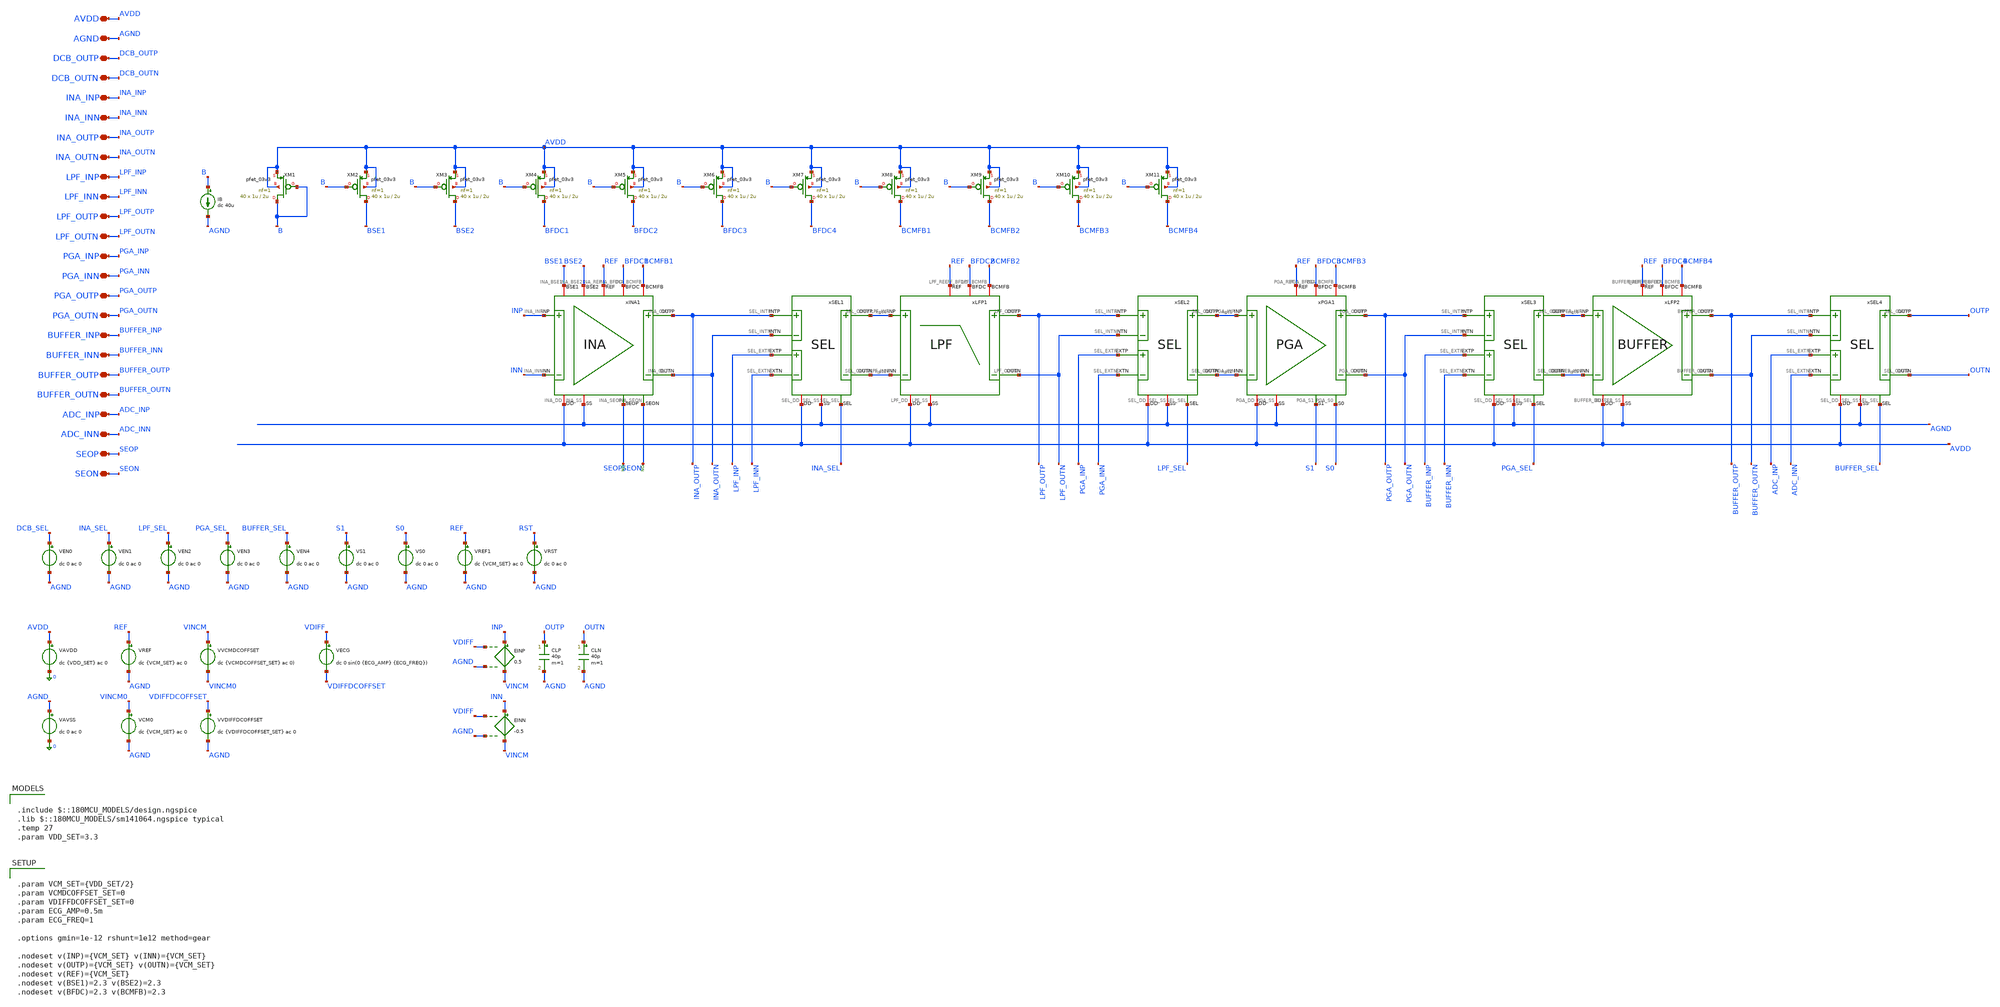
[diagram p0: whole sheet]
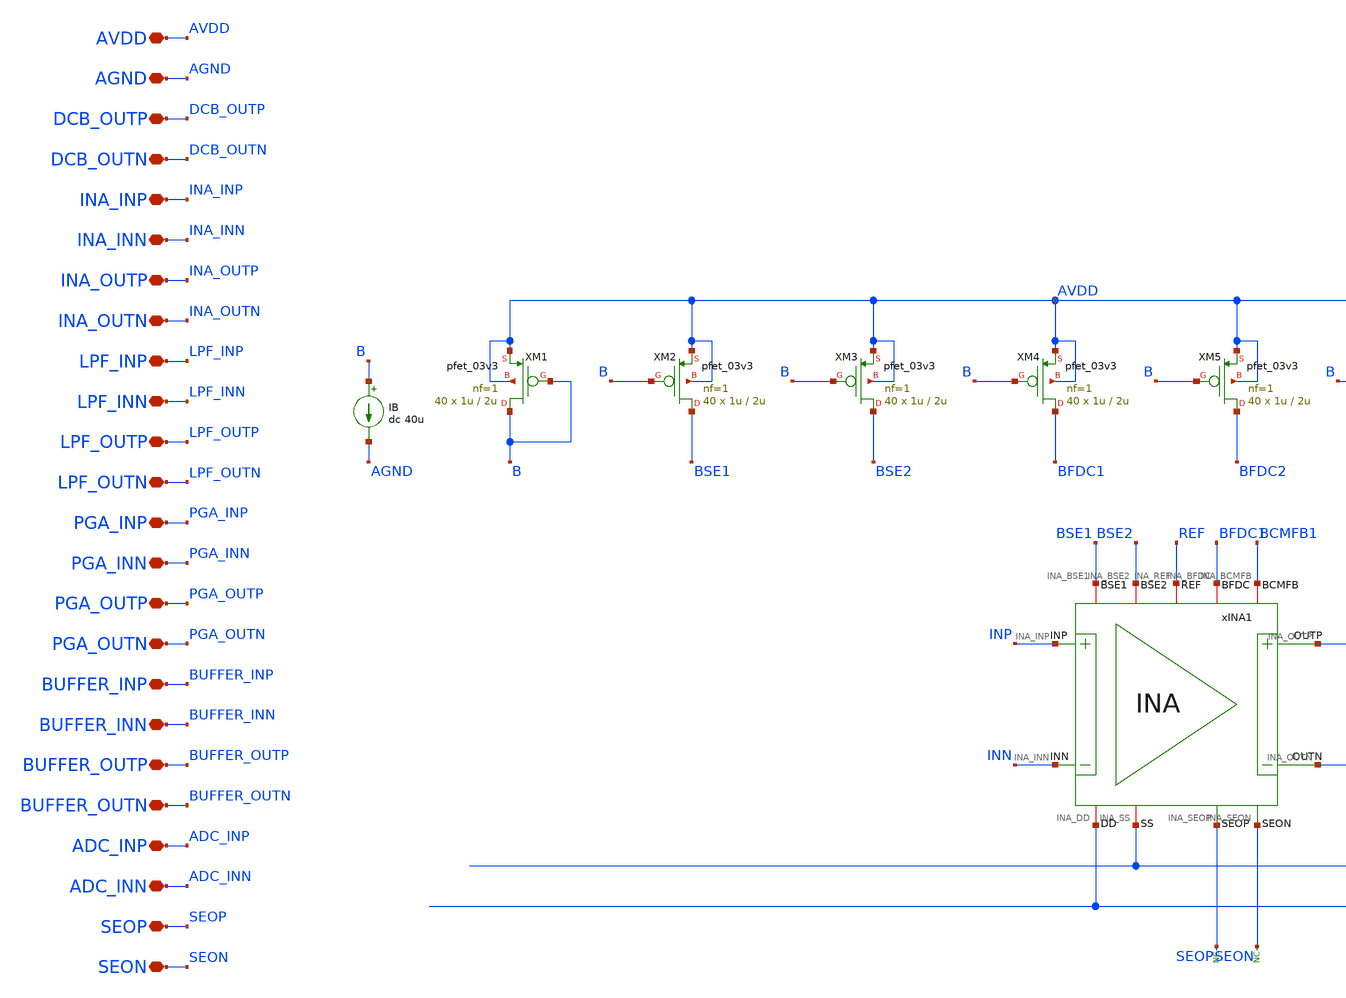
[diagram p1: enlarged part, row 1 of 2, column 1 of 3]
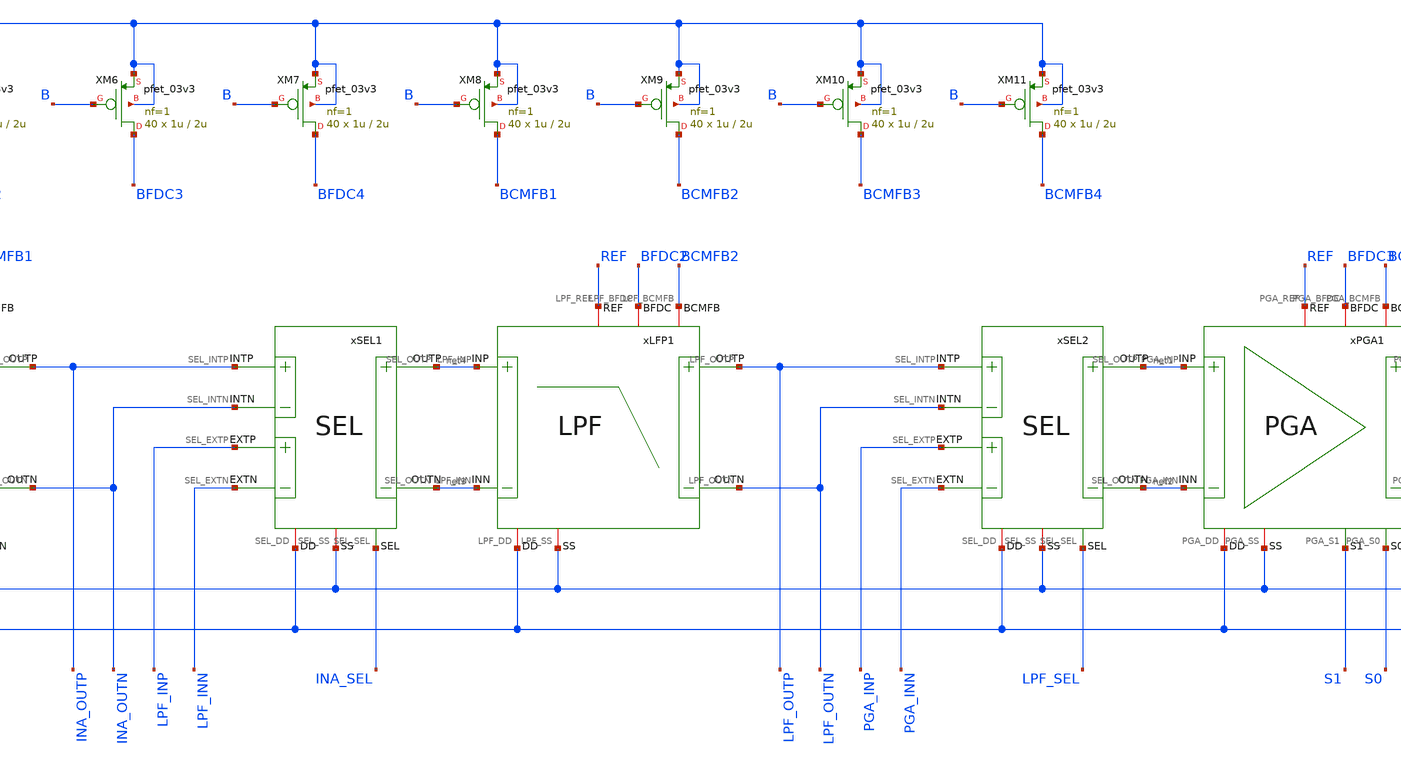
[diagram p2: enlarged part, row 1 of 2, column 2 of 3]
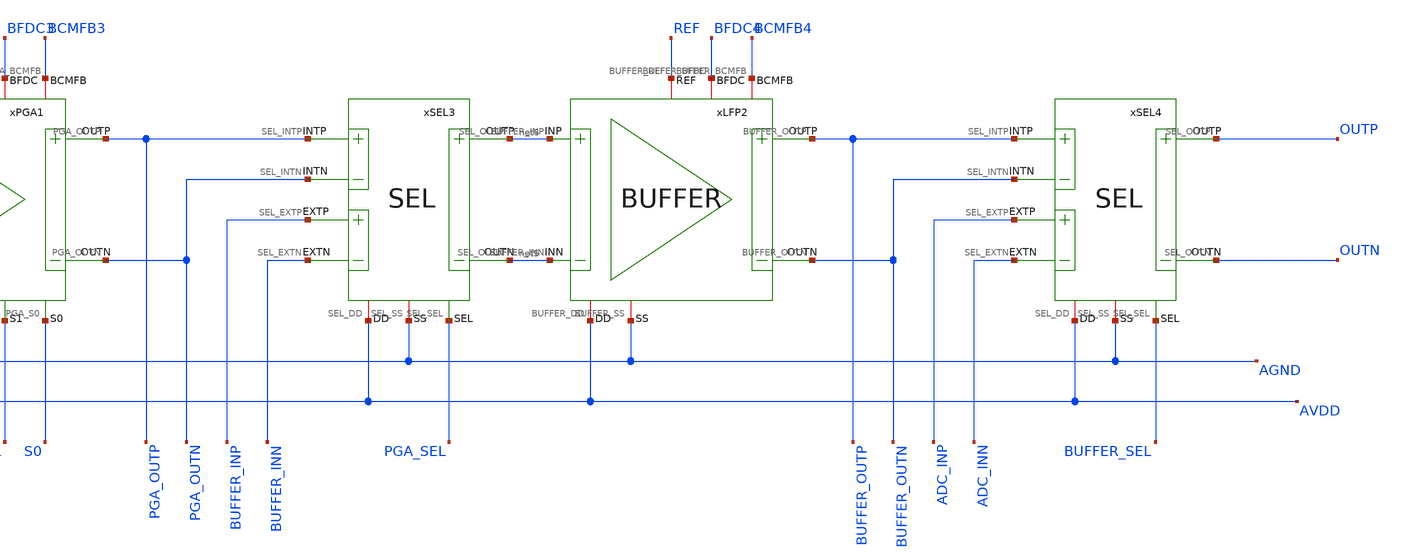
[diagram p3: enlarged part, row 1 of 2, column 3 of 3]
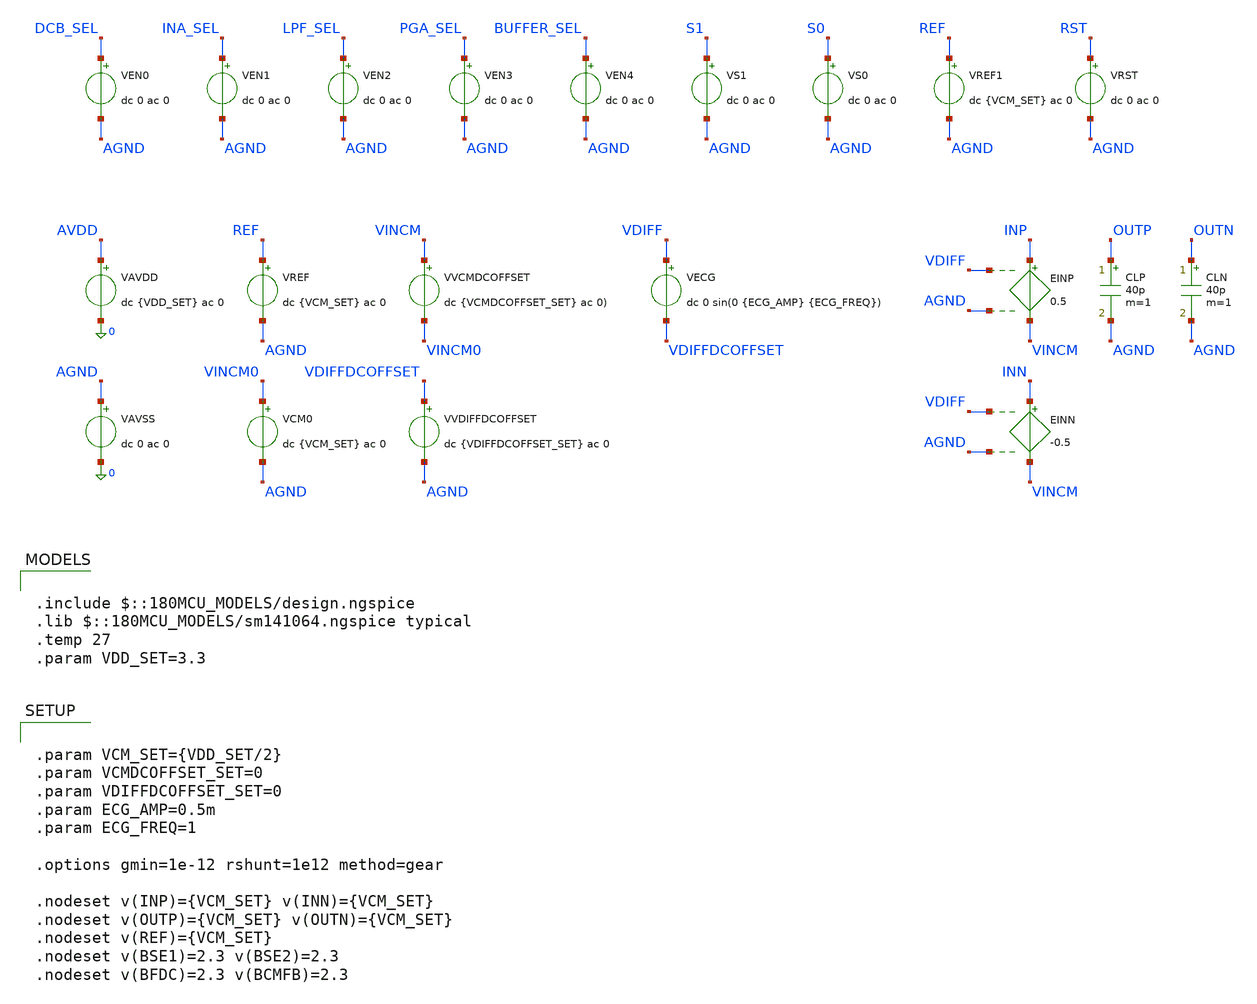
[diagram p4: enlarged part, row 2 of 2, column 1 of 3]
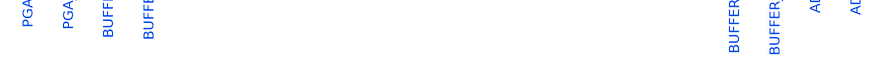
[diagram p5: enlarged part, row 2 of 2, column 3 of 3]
** sch_path: Design_Files/IC Design/Testbench/AFE/TRAN/AFE_TB_TRAN.sch
**.subckt AFE_TB_TRAN DCB_OUTP DCB_OUTN INA_INP INA_INN INA_OUTP INA_OUTN LPF_INP LPF_INN LPF_OUTP
*+ LPF_OUTN PGA_INP PGA_INN PGA_OUTP PGA_OUTN BUFFER_INP BUFFER_INN BUFFER_OUTP BUFFER_OUTN ADC_INP ADC_INN
*+ AVDD AGND SEOP SEON
*.iopin DCB_OUTP
*.iopin DCB_OUTN
*.iopin INA_INP
*.iopin INA_INN
*.iopin INA_OUTP
*.iopin INA_OUTN
*.iopin LPF_INP
*.iopin LPF_INN
*.iopin LPF_OUTP
*.iopin LPF_OUTN
*.iopin PGA_INP
*.iopin PGA_INN
*.iopin PGA_OUTP
*.iopin PGA_OUTN
*.iopin BUFFER_INP
*.iopin BUFFER_INN
*.iopin BUFFER_OUTP
*.iopin BUFFER_OUTN
*.iopin ADC_INP
*.iopin ADC_INN
*.iopin AVDD
*.iopin AGND
*.iopin SEOP
*.iopin SEON
VAVDD AVDD 0 dc {VDD_SET} ac 0
.save i(vavdd)
VAVSS AGND 0 dc 0 ac 0
.save i(vavss)
VREF REF AGND dc {VCM_SET} ac 0
CLP OUTP AGND 40p m=1
CLN OUTN AGND 40p m=1
EINP INP VINCM VDIFF AGND 0.5
EINN INN VINCM VDIFF AGND -0.5
VCM0 VINCM0 AGND dc {VCM_SET} ac 0
VVDIFFDCOFFSET VDIFFDCOFFSET AGND dc {VDIFFDCOFFSET_SET} ac 0
VVCMDCOFFSET VINCM VINCM0 dc {VCMDCOFFSET_SET} ac 0)
VECG VDIFF VDIFFDCOFFSET dc 0 sin(0 {ECG_AMP} {ECG_FREQ})
IB B AGND dc 40u
VREF1 REF AGND dc {VCM_SET} ac 0
XM1 B B AVDD AVDD pfet_03v3 L=2u W=1u nf=1 ad='int((nf+1)/2) * W/nf * 0.18u' as='int((nf+2)/2) * W/nf * 0.18u'
+ pd='2*int((nf+1)/2) * (W/nf + 0.18u)' ps='2*int((nf+2)/2) * (W/nf + 0.18u)' nrd='0.18u / W' nrs='0.18u / W'
+ sa=0 sb=0 sd=0 m=40
XM2 BSE1 B AVDD AVDD pfet_03v3 L=2u W=1u nf=1 ad='int((nf+1)/2) * W/nf * 0.18u' as='int((nf+2)/2) * W/nf * 0.18u'
+ pd='2*int((nf+1)/2) * (W/nf + 0.18u)' ps='2*int((nf+2)/2) * (W/nf + 0.18u)' nrd='0.18u / W' nrs='0.18u / W'
+ sa=0 sb=0 sd=0 m=40
XM3 BSE2 B AVDD AVDD pfet_03v3 L=2u W=1u nf=1 ad='int((nf+1)/2) * W/nf * 0.18u' as='int((nf+2)/2) * W/nf * 0.18u'
+ pd='2*int((nf+1)/2) * (W/nf + 0.18u)' ps='2*int((nf+2)/2) * (W/nf + 0.18u)' nrd='0.18u / W' nrs='0.18u / W'
+ sa=0 sb=0 sd=0 m=40
XM4 BFDC1 B AVDD AVDD pfet_03v3 L=2u W=1u nf=1 ad='int((nf+1)/2) * W/nf * 0.18u' as='int((nf+2)/2) * W/nf * 0.18u'
+ pd='2*int((nf+1)/2) * (W/nf + 0.18u)' ps='2*int((nf+2)/2) * (W/nf + 0.18u)' nrd='0.18u / W' nrs='0.18u / W'
+ sa=0 sb=0 sd=0 m=40
XM5 BFDC2 B AVDD AVDD pfet_03v3 L=2u W=1u nf=1 ad='int((nf+1)/2) * W/nf * 0.18u' as='int((nf+2)/2) * W/nf * 0.18u'
+ pd='2*int((nf+1)/2) * (W/nf + 0.18u)' ps='2*int((nf+2)/2) * (W/nf + 0.18u)' nrd='0.18u / W' nrs='0.18u / W'
+ sa=0 sb=0 sd=0 m=40
XM6 BFDC3 B AVDD AVDD pfet_03v3 L=2u W=1u nf=1 ad='int((nf+1)/2) * W/nf * 0.18u' as='int((nf+2)/2) * W/nf * 0.18u'
+ pd='2*int((nf+1)/2) * (W/nf + 0.18u)' ps='2*int((nf+2)/2) * (W/nf + 0.18u)' nrd='0.18u / W' nrs='0.18u / W'
+ sa=0 sb=0 sd=0 m=40
XM7 BFDC4 B AVDD AVDD pfet_03v3 L=2u W=1u nf=1 ad='int((nf+1)/2) * W/nf * 0.18u' as='int((nf+2)/2) * W/nf * 0.18u'
+ pd='2*int((nf+1)/2) * (W/nf + 0.18u)' ps='2*int((nf+2)/2) * (W/nf + 0.18u)' nrd='0.18u / W' nrs='0.18u / W'
+ sa=0 sb=0 sd=0 m=40
XM8 BCMFB1 B AVDD AVDD pfet_03v3 L=2u W=1u nf=1 ad='int((nf+1)/2) * W/nf * 0.18u' as='int((nf+2)/2) * W/nf * 0.18u'
+ pd='2*int((nf+1)/2) * (W/nf + 0.18u)' ps='2*int((nf+2)/2) * (W/nf + 0.18u)' nrd='0.18u / W' nrs='0.18u / W'
+ sa=0 sb=0 sd=0 m=40
XM9 BCMFB2 B AVDD AVDD pfet_03v3 L=2u W=1u nf=1 ad='int((nf+1)/2) * W/nf * 0.18u' as='int((nf+2)/2) * W/nf * 0.18u'
+ pd='2*int((nf+1)/2) * (W/nf + 0.18u)' ps='2*int((nf+2)/2) * (W/nf + 0.18u)' nrd='0.18u / W' nrs='0.18u / W'
+ sa=0 sb=0 sd=0 m=40
xLFP1 AVDD AGND net4 net3 LPF_OUTN BFDC2 LPF_OUTP BCMFB2 REF LPF
xPGA1 AVDD AGND net1 net2 PGA_OUTN BFDC3 PGA_OUTP BCMFB3 REF S1 S0 PGA
xSEL1 AVDD AGND INA_OUTP INA_OUTN net3 net4 LPF_INP LPF_INN INA_SEL SEL
xINA1 AVDD AGND INP INN INA_OUTN BFDC1 INA_OUTP BCMFB1 REF SEON SEOP BSE1 BSE2 INA
xSEL2 AVDD AGND LPF_OUTP LPF_OUTN net2 net1 PGA_INP PGA_INN LPF_SEL SEL
xSEL3 AVDD AGND PGA_OUTP PGA_OUTN net5 net6 BUFFER_INP BUFFER_INN PGA_SEL SEL
xSEL4 AVDD AGND BUFFER_OUTP BUFFER_OUTN OUTN OUTP ADC_INP ADC_INN BUFFER_SEL SEL
xLFP2 AVDD AGND net6 net5 BUFFER_OUTN BFDC4 BUFFER_OUTP BCMFB4 REF BUFFER
XM10 BCMFB3 B AVDD AVDD pfet_03v3 L=2u W=1u nf=1 ad='int((nf+1)/2) * W/nf * 0.18u' as='int((nf+2)/2) * W/nf * 0.18u'
+ pd='2*int((nf+1)/2) * (W/nf + 0.18u)' ps='2*int((nf+2)/2) * (W/nf + 0.18u)' nrd='0.18u / W' nrs='0.18u / W'
+ sa=0 sb=0 sd=0 m=40
XM11 BCMFB4 B AVDD AVDD pfet_03v3 L=2u W=1u nf=1 ad='int((nf+1)/2) * W/nf * 0.18u' as='int((nf+2)/2) * W/nf * 0.18u'
+ pd='2*int((nf+1)/2) * (W/nf + 0.18u)' ps='2*int((nf+2)/2) * (W/nf + 0.18u)' nrd='0.18u / W' nrs='0.18u / W'
+ sa=0 sb=0 sd=0 m=40
VEN1 INA_SEL AGND dc 0 ac 0
.save i(ven1)
VS0 S0 AGND dc 0 ac 0
.save i(vs0)
VS1 S1 AGND dc 0 ac 0
.save i(vs1)
* noconn SEON
* noconn SEOP
VEN2 LPF_SEL AGND dc 0 ac 0
.save i(ven2)
VEN3 PGA_SEL AGND dc 0 ac 0
.save i(ven3)
VEN4 BUFFER_SEL AGND dc 0 ac 0
.save i(ven4)
VEN0 DCB_SEL AGND dc 0 ac 0
.save i(ven0)
VRST RST AGND dc 0 ac 0
.save i(vrst)
**** begin user architecture code

.include $::180MCU_MODELS/design.ngspice
.lib $::180MCU_MODELS/sm141064.ngspice typical
.temp 27
.param VDD_SET=3.3



.param VCM_SET={VDD_SET/2}
.param VCMDCOFFSET_SET=0
.param VDIFFDCOFFSET_SET=0
.param ECG_AMP=0.5m
.param ECG_FREQ=1

.options gmin=1e-12 rshunt=1e12 method=gear

.nodeset v(INP)={VCM_SET} v(INN)={VCM_SET}
.nodeset v(OUTP)={VCM_SET} v(OUTN)={VCM_SET}
.nodeset v(REF)={VCM_SET}
.nodeset v(BSE1)=2.3 v(BSE2)=2.3
.nodeset v(BFDC)=2.3 v(BCMFB)=2.3





.control
destroy all
save all
set wr_vecnames
set wr_singlescale
option numdgt=15

shell mkdir -p /foss/designs/ECG_Acquisition_IC/Measurement_Results/IC_Simulation/AFE/NOM.Result_txt
shell rm -f
+ /foss/designs/ECG_Acquisition_IC/Measurement_Results/IC_Simulation/AFE/NOM.Result_txt/NOM.tran_*.txt


* VCM DC offset, 0.5m
alterparam VCMDCOFFSET_SET = 300m
alterparam VDIFFDCOFFSET_SET = 0
alterparam ECG_AMP = 0.5m
reset
save all
set wr_vecnames
set wr_singlescale
option numdgt=15
tran 0.5m 3
let tr_vcmdcoffset = v(VINCM)-v(VINCM0)
let tr_vdiffdcoffset = v(VDIFFDCOFFSET)-v(AGND)
let tr_vin_cm = 0.5*(v(INP)+v(INN))-v(AGND)
let tr_vin_diff = v(INP)-v(INN)
let tr_vout_cm = 0.5*(v(OUTP)+v(OUTN))-v(AGND)
let tr_vout_diff = v(OUTP)-v(OUTN)
let tr_idd = -vavdd#branch
setscale time
wrdata
+ /foss/designs/ECG_Acquisition_IC/Measurement_Results/IC_Simulation/AFE/NOM.Result_txt/NOM.tran_vcmdcoffset_p300m_0p5m.txt tr_vcmdcoffset tr_vdiffdcoffset tr_vin_cm tr_vin_diff v(INP) v(INN) v(OUTP) v(OUTN) tr_vout_cm
+ tr_vout_diff tr_idd

alterparam VCMDCOFFSET_SET = 500m
alterparam VDIFFDCOFFSET_SET = 0
alterparam ECG_AMP = 0.5m
reset
save all
set wr_vecnames
set wr_singlescale
option numdgt=15
tran 0.5m 3
let tr_vcmdcoffset = v(VINCM)-v(VINCM0)
let tr_vdiffdcoffset = v(VDIFFDCOFFSET)-v(AGND)
let tr_vin_cm = 0.5*(v(INP)+v(INN))-v(AGND)
let tr_vin_diff = v(INP)-v(INN)
let tr_vout_cm = 0.5*(v(OUTP)+v(OUTN))-v(AGND)
let tr_vout_diff = v(OUTP)-v(OUTN)
let tr_idd = -vavdd#branch
setscale time
wrdata
+ /foss/designs/ECG_Acquisition_IC/Measurement_Results/IC_Simulation/AFE/NOM.Result_txt/NOM.tran_vcmdcoffset_p500m_0p5m.txt tr_vcmdcoffset tr_vdiffdcoffset tr_vin_cm tr_vin_diff v(INP) v(INN) v(OUTP) v(OUTN) tr_vout_cm
+ tr_vout_diff tr_idd

alterparam VCMDCOFFSET_SET = 0
alterparam VDIFFDCOFFSET_SET = 0
alterparam ECG_AMP = 0.5m
reset
save all
set wr_vecnames
set wr_singlescale
option numdgt=15
tran 0.5m 3
let tr_vcmdcoffset = v(VINCM)-v(VINCM0)
let tr_vdiffdcoffset = v(VDIFFDCOFFSET)-v(AGND)
let tr_vin_cm = 0.5*(v(INP)+v(INN))-v(AGND)
let tr_vin_diff = v(INP)-v(INN)
let tr_vout_cm = 0.5*(v(OUTP)+v(OUTN))-v(AGND)
let tr_vout_diff = v(OUTP)-v(OUTN)
let tr_idd = -vavdd#branch
setscale time
wrdata
+ /foss/designs/ECG_Acquisition_IC/Measurement_Results/IC_Simulation/AFE/NOM.Result_txt/NOM.tran_vcmdcoffset_0_0p5m.txt tr_vcmdcoffset tr_vdiffdcoffset tr_vin_cm tr_vin_diff v(INP) v(INN) v(OUTP) v(OUTN) tr_vout_cm
+ tr_vout_diff tr_idd

alterparam VCMDCOFFSET_SET = -300m
alterparam VDIFFDCOFFSET_SET = 0
alterparam ECG_AMP = 0.5m
reset
save all
set wr_vecnames
set wr_singlescale
option numdgt=15
tran 0.5m 3
let tr_vcmdcoffset = v(VINCM)-v(VINCM0)
let tr_vdiffdcoffset = v(VDIFFDCOFFSET)-v(AGND)
let tr_vin_cm = 0.5*(v(INP)+v(INN))-v(AGND)
let tr_vin_diff = v(INP)-v(INN)
let tr_vout_cm = 0.5*(v(OUTP)+v(OUTN))-v(AGND)
let tr_vout_diff = v(OUTP)-v(OUTN)
let tr_idd = -vavdd#branch
setscale time
wrdata
+ /foss/designs/ECG_Acquisition_IC/Measurement_Results/IC_Simulation/AFE/NOM.Result_txt/NOM.tran_vcmdcoffset_n300m_0p5m.txt tr_vcmdcoffset tr_vdiffdcoffset tr_vin_cm tr_vin_diff v(INP) v(INN) v(OUTP) v(OUTN) tr_vout_cm
+ tr_vout_diff tr_idd

alterparam VCMDCOFFSET_SET = -500m
alterparam VDIFFDCOFFSET_SET = 0
alterparam ECG_AMP = 0.5m
reset
save all
set wr_vecnames
set wr_singlescale
option numdgt=15
tran 0.5m 3
let tr_vcmdcoffset = v(VINCM)-v(VINCM0)
let tr_vdiffdcoffset = v(VDIFFDCOFFSET)-v(AGND)
let tr_vin_cm = 0.5*(v(INP)+v(INN))-v(AGND)
let tr_vin_diff = v(INP)-v(INN)
let tr_vout_cm = 0.5*(v(OUTP)+v(OUTN))-v(AGND)
let tr_vout_diff = v(OUTP)-v(OUTN)
let tr_idd = -vavdd#branch
setscale time
wrdata
+ /foss/designs/ECG_Acquisition_IC/Measurement_Results/IC_Simulation/AFE/NOM.Result_txt/NOM.tran_vcmdcoffset_n500m_0p5m.txt tr_vcmdcoffset tr_vdiffdcoffset tr_vin_cm tr_vin_diff v(INP) v(INN) v(OUTP) v(OUTN) tr_vout_cm
+ tr_vout_diff tr_idd


* VCM DC offset, 5m
alterparam VCMDCOFFSET_SET = 300m
alterparam VDIFFDCOFFSET_SET = 0
alterparam ECG_AMP = 5m
reset
save all
set wr_vecnames
set wr_singlescale
option numdgt=15
tran 0.5m 3
let tr_vcmdcoffset = v(VINCM)-v(VINCM0)
let tr_vdiffdcoffset = v(VDIFFDCOFFSET)-v(AGND)
let tr_vin_cm = 0.5*(v(INP)+v(INN))-v(AGND)
let tr_vin_diff = v(INP)-v(INN)
let tr_vout_cm = 0.5*(v(OUTP)+v(OUTN))-v(AGND)
let tr_vout_diff = v(OUTP)-v(OUTN)
let tr_idd = -vavdd#branch
setscale time
wrdata
+ /foss/designs/ECG_Acquisition_IC/Measurement_Results/IC_Simulation/AFE/NOM.Result_txt/NOM.tran_vcmdcoffset_p300m_5m.txt tr_vcmdcoffset tr_vdiffdcoffset tr_vin_cm tr_vin_diff v(INP) v(INN) v(OUTP) v(OUTN) tr_vout_cm
+ tr_vout_diff tr_idd

alterparam VCMDCOFFSET_SET = 500m
alterparam VDIFFDCOFFSET_SET = 0
alterparam ECG_AMP = 5m
reset
save all
set wr_vecnames
set wr_singlescale
option numdgt=15
tran 0.5m 3
let tr_vcmdcoffset = v(VINCM)-v(VINCM0)
let tr_vdiffdcoffset = v(VDIFFDCOFFSET)-v(AGND)
let tr_vin_cm = 0.5*(v(INP)+v(INN))-v(AGND)
let tr_vin_diff = v(INP)-v(INN)
let tr_vout_cm = 0.5*(v(OUTP)+v(OUTN))-v(AGND)
let tr_vout_diff = v(OUTP)-v(OUTN)
let tr_idd = -vavdd#branch
setscale time
wrdata
+ /foss/designs/ECG_Acquisition_IC/Measurement_Results/IC_Simulation/AFE/NOM.Result_txt/NOM.tran_vcmdcoffset_p500m_5m.txt tr_vcmdcoffset tr_vdiffdcoffset tr_vin_cm tr_vin_diff v(INP) v(INN) v(OUTP) v(OUTN) tr_vout_cm
+ tr_vout_diff tr_idd

alterparam VCMDCOFFSET_SET = 0
alterparam VDIFFDCOFFSET_SET = 0
alterparam ECG_AMP = 5m
reset
save all
set wr_vecnames
set wr_singlescale
option numdgt=15
tran 0.5m 3
let tr_vcmdcoffset = v(VINCM)-v(VINCM0)
let tr_vdiffdcoffset = v(VDIFFDCOFFSET)-v(AGND)
let tr_vin_cm = 0.5*(v(INP)+v(INN))-v(AGND)
let tr_vin_diff = v(INP)-v(INN)
let tr_vout_cm = 0.5*(v(OUTP)+v(OUTN))-v(AGND)
let tr_vout_diff = v(OUTP)-v(OUTN)
let tr_idd = -vavdd#branch
setscale time
wrdata
+ /foss/designs/ECG_Acquisition_IC/Measurement_Results/IC_Simulation/AFE/NOM.Result_txt/NOM.tran_vcmdcoffset_0_5m.txt tr_vcmdcoffset tr_vdiffdcoffset tr_vin_cm tr_vin_diff v(INP) v(INN) v(OUTP) v(OUTN) tr_vout_cm
+ tr_vout_diff tr_idd

alterparam VCMDCOFFSET_SET = -300m
alterparam VDIFFDCOFFSET_SET = 0
alterparam ECG_AMP = 5m
reset
save all
set wr_vecnames
set wr_singlescale
option numdgt=15
tran 0.5m 3
let tr_vcmdcoffset = v(VINCM)-v(VINCM0)
let tr_vdiffdcoffset = v(VDIFFDCOFFSET)-v(AGND)
let tr_vin_cm = 0.5*(v(INP)+v(INN))-v(AGND)
let tr_vin_diff = v(INP)-v(INN)
let tr_vout_cm = 0.5*(v(OUTP)+v(OUTN))-v(AGND)
let tr_vout_diff = v(OUTP)-v(OUTN)
let tr_idd = -vavdd#branch
setscale time
wrdata
+ /foss/designs/ECG_Acquisition_IC/Measurement_Results/IC_Simulation/AFE/NOM.Result_txt/NOM.tran_vcmdcoffset_n300m_5m.txt tr_vcmdcoffset tr_vdiffdcoffset tr_vin_cm tr_vin_diff v(INP) v(INN) v(OUTP) v(OUTN) tr_vout_cm
+ tr_vout_diff tr_idd

alterparam VCMDCOFFSET_SET = -500m
alterparam VDIFFDCOFFSET_SET = 0
alterparam ECG_AMP = 5m
reset
save all
set wr_vecnames
set wr_singlescale
option numdgt=15
tran 0.5m 3
let tr_vcmdcoffset = v(VINCM)-v(VINCM0)
let tr_vdiffdcoffset = v(VDIFFDCOFFSET)-v(AGND)
let tr_vin_cm = 0.5*(v(INP)+v(INN))-v(AGND)
let tr_vin_diff = v(INP)-v(INN)
let tr_vout_cm = 0.5*(v(OUTP)+v(OUTN))-v(AGND)
let tr_vout_diff = v(OUTP)-v(OUTN)
let tr_idd = -vavdd#branch
setscale time
wrdata
+ /foss/designs/ECG_Acquisition_IC/Measurement_Results/IC_Simulation/AFE/NOM.Result_txt/NOM.tran_vcmdcoffset_n500m_5m.txt tr_vcmdcoffset tr_vdiffdcoffset tr_vin_cm tr_vin_diff v(INP) v(INN) v(OUTP) v(OUTN) tr_vout_cm
+ tr_vout_diff tr_idd


* VDIFF DC offset, 0.5m
alterparam VCMDCOFFSET_SET = 0
alterparam VDIFFDCOFFSET_SET = 300m
alterparam ECG_AMP = 0.5m
reset
save all
set wr_vecnames
set wr_singlescale
option numdgt=15
tran 0.5m 3
let tr_vcmdcoffset = v(VINCM)-v(VINCM0)
let tr_vdiffdcoffset = v(VDIFFDCOFFSET)-v(AGND)
let tr_vin_cm = 0.5*(v(INP)+v(INN))-v(AGND)
let tr_vin_diff = v(INP)-v(INN)
let tr_vout_cm = 0.5*(v(OUTP)+v(OUTN))-v(AGND)
let tr_vout_diff = v(OUTP)-v(OUTN)
let tr_idd = -vavdd#branch
setscale time
wrdata
+ /foss/designs/ECG_Acquisition_IC/Measurement_Results/IC_Simulation/AFE/NOM.Result_txt/NOM.tran_vdiffdcoffset_p300m_0p5m.txt tr_vcmdcoffset tr_vdiffdcoffset tr_vin_cm tr_vin_diff v(INP) v(INN) v(OUTP) v(OUTN) tr_vout_cm
+ tr_vout_diff tr_idd

alterparam VCMDCOFFSET_SET = 0
alterparam VDIFFDCOFFSET_SET = 500m
alterparam ECG_AMP = 0.5m
reset
save all
set wr_vecnames
set wr_singlescale
option numdgt=15
tran 0.5m 3
let tr_vcmdcoffset = v(VINCM)-v(VINCM0)
let tr_vdiffdcoffset = v(VDIFFDCOFFSET)-v(AGND)
let tr_vin_cm = 0.5*(v(INP)+v(INN))-v(AGND)
let tr_vin_diff = v(INP)-v(INN)
let tr_vout_cm = 0.5*(v(OUTP)+v(OUTN))-v(AGND)
let tr_vout_diff = v(OUTP)-v(OUTN)
let tr_idd = -vavdd#branch
setscale time
wrdata
+ /foss/designs/ECG_Acquisition_IC/Measurement_Results/IC_Simulation/AFE/NOM.Result_txt/NOM.tran_vdiffdcoffset_p500m_0p5m.txt tr_vcmdcoffset tr_vdiffdcoffset tr_vin_cm tr_vin_diff v(INP) v(INN) v(OUTP) v(OUTN) tr_vout_cm
+ tr_vout_diff tr_idd

alterparam VCMDCOFFSET_SET = 0
alterparam VDIFFDCOFFSET_SET = 0
alterparam ECG_AMP = 0.5m
reset
save all
set wr_vecnames
set wr_singlescale
option numdgt=15
tran 0.5m 3
let tr_vcmdcoffset = v(VINCM)-v(VINCM0)
let tr_vdiffdcoffset = v(VDIFFDCOFFSET)-v(AGND)
let tr_vin_cm = 0.5*(v(INP)+v(INN))-v(AGND)
let tr_vin_diff = v(INP)-v(INN)
let tr_vout_cm = 0.5*(v(OUTP)+v(OUTN))-v(AGND)
let tr_vout_diff = v(OUTP)-v(OUTN)
let tr_idd = -vavdd#branch
setscale time
wrdata
+ /foss/designs/ECG_Acquisition_IC/Measurement_Results/IC_Simulation/AFE/NOM.Result_txt/NOM.tran_vdiffdcoffset_0_0p5m.txt tr_vcmdcoffset tr_vdiffdcoffset tr_vin_cm tr_vin_diff v(INP) v(INN) v(OUTP) v(OUTN) tr_vout_cm
+ tr_vout_diff tr_idd

alterparam VCMDCOFFSET_SET = 0
alterparam VDIFFDCOFFSET_SET = -300m
alterparam ECG_AMP = 0.5m
reset
save all
set wr_vecnames
set wr_singlescale
option numdgt=15
tran 0.5m 3
let tr_vcmdcoffset = v(VINCM)-v(VINCM0)
let tr_vdiffdcoffset = v(VDIFFDCOFFSET)-v(AGND)
let tr_vin_cm = 0.5*(v(INP)+v(INN))-v(AGND)
let tr_vin_diff = v(INP)-v(INN)
let tr_vout_cm = 0.5*(v(OUTP)+v(OUTN))-v(AGND)
let tr_vout_diff = v(OUTP)-v(OUTN)
let tr_idd = -vavdd#branch
setscale time
wrdata
+ /foss/designs/ECG_Acquisition_IC/Measurement_Results/IC_Simulation/AFE/NOM.Result_txt/NOM.tran_vdiffdcoffset_n300m_0p5m.txt tr_vcmdcoffset tr_vdiffdcoffset tr_vin_cm tr_vin_diff v(INP) v(INN) v(OUTP) v(OUTN) tr_vout_cm
+ tr_vout_diff tr_idd

alterparam VCMDCOFFSET_SET = 0
alterparam VDIFFDCOFFSET_SET = -500m
alterparam ECG_AMP = 0.5m
reset
save all
set wr_vecnames
set wr_singlescale
option numdgt=15
tran 0.5m 3
let tr_vcmdcoffset = v(VINCM)-v(VINCM0)
let tr_vdiffdcoffset = v(VDIFFDCOFFSET)-v(AGND)
let tr_vin_cm = 0.5*(v(INP)+v(INN))-v(AGND)
let tr_vin_diff = v(INP)-v(INN)
let tr_vout_cm = 0.5*(v(OUTP)+v(OUTN))-v(AGND)
let tr_vout_diff = v(OUTP)-v(OUTN)
let tr_idd = -vavdd#branch
setscale time
wrdata
+ /foss/designs/ECG_Acquisition_IC/Measurement_Results/IC_Simulation/AFE/NOM.Result_txt/NOM.tran_vdiffdcoffset_n500m_0p5m.txt tr_vcmdcoffset tr_vdiffdcoffset tr_vin_cm tr_vin_diff v(INP) v(INN) v(OUTP) v(OUTN) tr_vout_cm
+ tr_vout_diff tr_idd


* VDIFF DC offset, 5m
alterparam VCMDCOFFSET_SET = 0
alterparam VDIFFDCOFFSET_SET = 300m
alterparam ECG_AMP = 5m
reset
save all
set wr_vecnames
set wr_singlescale
option numdgt=15
tran 0.5m 3
let tr_vcmdcoffset = v(VINCM)-v(VINCM0)
let tr_vdiffdcoffset = v(VDIFFDCOFFSET)-v(AGND)
let tr_vin_cm = 0.5*(v(INP)+v(INN))-v(AGND)
let tr_vin_diff = v(INP)-v(INN)
let tr_vout_cm = 0.5*(v(OUTP)+v(OUTN))-v(AGND)
let tr_vout_diff = v(OUTP)-v(OUTN)
let tr_idd = -vavdd#branch
setscale time
wrdata
+ /foss/designs/ECG_Acquisition_IC/Measurement_Results/IC_Simulation/AFE/NOM.Result_txt/NOM.tran_vdiffdcoffset_p300m_5m.txt tr_vcmdcoffset tr_vdiffdcoffset tr_vin_cm tr_vin_diff v(INP) v(INN) v(OUTP) v(OUTN) tr_vout_cm
+ tr_vout_diff tr_idd

alterparam VCMDCOFFSET_SET = 0
alterparam VDIFFDCOFFSET_SET = 500m
alterparam ECG_AMP = 5m
reset
save all
set wr_vecnames
set wr_singlescale
option numdgt=15
tran 0.5m 3
let tr_vcmdcoffset = v(VINCM)-v(VINCM0)
let tr_vdiffdcoffset = v(VDIFFDCOFFSET)-v(AGND)
let tr_vin_cm = 0.5*(v(INP)+v(INN))-v(AGND)
let tr_vin_diff = v(INP)-v(INN)
let tr_vout_cm = 0.5*(v(OUTP)+v(OUTN))-v(AGND)
let tr_vout_diff = v(OUTP)-v(OUTN)
let tr_idd = -vavdd#branch
setscale time
wrdata
+ /foss/designs/ECG_Acquisition_IC/Measurement_Results/IC_Simulation/AFE/NOM.Result_txt/NOM.tran_vdiffdcoffset_p500m_5m.txt tr_vcmdcoffset tr_vdiffdcoffset tr_vin_cm tr_vin_diff v(INP) v(INN) v(OUTP) v(OUTN) tr_vout_cm
+ tr_vout_diff tr_idd

alterparam VCMDCOFFSET_SET = 0
alterparam VDIFFDCOFFSET_SET = 0
alterparam ECG_AMP = 5m
reset
save all
set wr_vecnames
set wr_singlescale
option numdgt=15
tran 0.5m 3
let tr_vcmdcoffset = v(VINCM)-v(VINCM0)
let tr_vdiffdcoffset = v(VDIFFDCOFFSET)-v(AGND)
let tr_vin_cm = 0.5*(v(INP)+v(INN))-v(AGND)
let tr_vin_diff = v(INP)-v(INN)
let tr_vout_cm = 0.5*(v(OUTP)+v(OUTN))-v(AGND)
let tr_vout_diff = v(OUTP)-v(OUTN)
let tr_idd = -vavdd#branch
setscale time
wrdata
+ /foss/designs/ECG_Acquisition_IC/Measurement_Results/IC_Simulation/AFE/NOM.Result_txt/NOM.tran_vdiffdcoffset_0_5m.txt tr_vcmdcoffset tr_vdiffdcoffset tr_vin_cm tr_vin_diff v(INP) v(INN) v(OUTP) v(OUTN) tr_vout_cm
+ tr_vout_diff tr_idd

alterparam VCMDCOFFSET_SET = 0
alterparam VDIFFDCOFFSET_SET = -300m
alterparam ECG_AMP = 5m
reset
save all
set wr_vecnames
set wr_singlescale
option numdgt=15
tran 0.5m 3
let tr_vcmdcoffset = v(VINCM)-v(VINCM0)
let tr_vdiffdcoffset = v(VDIFFDCOFFSET)-v(AGND)
let tr_vin_cm = 0.5*(v(INP)+v(INN))-v(AGND)
let tr_vin_diff = v(INP)-v(INN)
let tr_vout_cm = 0.5*(v(OUTP)+v(OUTN))-v(AGND)
let tr_vout_diff = v(OUTP)-v(OUTN)
let tr_idd = -vavdd#branch
setscale time
wrdata
+ /foss/designs/ECG_Acquisition_IC/Measurement_Results/IC_Simulation/AFE/NOM.Result_txt/NOM.tran_vdiffdcoffset_n300m_5m.txt tr_vcmdcoffset tr_vdiffdcoffset tr_vin_cm tr_vin_diff v(INP) v(INN) v(OUTP) v(OUTN) tr_vout_cm
+ tr_vout_diff tr_idd

alterparam VCMDCOFFSET_SET = 0
alterparam VDIFFDCOFFSET_SET = -500m
alterparam ECG_AMP = 5m
reset
save all
set wr_vecnames
set wr_singlescale
option numdgt=15
tran 0.5m 3
let tr_vcmdcoffset = v(VINCM)-v(VINCM0)
let tr_vdiffdcoffset = v(VDIFFDCOFFSET)-v(AGND)
let tr_vin_cm = 0.5*(v(INP)+v(INN))-v(AGND)
let tr_vin_diff = v(INP)-v(INN)
let tr_vout_cm = 0.5*(v(OUTP)+v(OUTN))-v(AGND)
let tr_vout_diff = v(OUTP)-v(OUTN)
let tr_idd = -vavdd#branch
setscale time
wrdata
+ /foss/designs/ECG_Acquisition_IC/Measurement_Results/IC_Simulation/AFE/NOM.Result_txt/NOM.tran_vdiffdcoffset_n500m_5m.txt tr_vcmdcoffset tr_vdiffdcoffset tr_vin_cm tr_vin_diff v(INP) v(INN) v(OUTP) v(OUTN) tr_vout_cm
+ tr_vout_diff tr_idd

quit
.endc


**** end user architecture code
**.ends

* expanding   symbol:  ECG_Acquisition_IC/Design_Files/IC Design/Schematic/LPF/LPF.sym # of pins=9
** sym_path: Design_Files/IC Design/Schematic/LPF/LPF.sym
** sch_path: Design_Files/IC Design/Schematic/LPF/LPF.sch
.subckt LPF LPF_DD LPF_SS LPF_INP LPF_INN LPF_OUTN LPF_BFDC LPF_OUTP LPF_BCMFB LPF_REF
*.iopin LPF_DD
*.iopin LPF_SS
*.ipin LPF_INP
*.ipin LPF_INN
*.opin LPF_OUTP
*.iopin LPF_BFDC
*.opin LPF_OUTN
*.iopin LPF_BCMFB
*.iopin LPF_REF
RFBP net1 LPF_OUTN 3.7Meg m=1
xFDOTA1 LPF_DD LPF_SS net1 net2 LPF_OUTN LPF_BFDC LPF_OUTP LPF_BCMFB LPF_REF LPF_VOCM FD_OTA
RINN LPF_INN net2 3.7Meg m=1
RINP LPF_INP net1 3.7Meg m=1
RFBN net2 LPF_OUTP 3.7Meg m=1
CLPFP net1 LPF_OUTN 20p m=5
CLPFN net2 LPF_OUTP 20p m=5
.ends


* expanding   symbol:  ECG_Acquisition_IC/Design_Files/IC Design/Schematic/PGA/PGA.sym # of pins=11
** sym_path: Design_Files/IC Design/Schematic/PGA/PGA.sym
** sch_path: Design_Files/IC Design/Schematic/PGA/PGA.sch
.subckt PGA PGA_DD PGA_SS PGA_INP PGA_INN PGA_OUTN PGA_BFDC PGA_OUTP PGA_BCMFB PGA_REF PGA_S1 PGA_S0
*.iopin PGA_DD
*.iopin PGA_SS
*.ipin PGA_INP
*.ipin PGA_INN
*.opin PGA_OUTP
*.iopin PGA_BFDC
*.opin PGA_OUTN
*.iopin PGA_BCMFB
*.iopin PGA_REF
*.ipin PGA_S0
*.ipin PGA_S1
RFBP1 net2 net1 40k m=1
xFDOTA1 PGA_DD PGA_SS net2 net8 PGA_OUTN PGA_BFDC PGA_OUTP PGA_BCMFB PGA_REF PGA_VOCM FD_OTA
RFBP2 net1 net3 40k m=1
RFBP3 net3 net4 120k m=1
RFBP4 net4 PGA_OUTN 120k m=1
RINN PGA_INN net8 20k m=1
RINP PGA_INP net2 20k m=1
xTG1 PGA_DD PGA_SS net1 net3 S0B PGA_S0 TG
xTG3 PGA_DD PGA_SS net3 PGA_OUTN S1B PGA_S1 TG
xINV1 PGA_DD PGA_SS PGA_S0 S0B INV
xTG2 PGA_DD PGA_SS net3 net4 S0B PGA_S0 TG
RFBN1 net8 net5 40k m=1
RFBN2 net5 net6 40k m=1
RFBN3 net6 net7 120k m=1
RFBN4 net7 PGA_OUTP 120k m=1
xTG4 PGA_DD PGA_SS net5 net6 S0B PGA_S0 TG
xTG5 PGA_DD PGA_SS net6 net7 S0B PGA_S0 TG
xINV2 PGA_DD PGA_SS PGA_S1 S1B INV
xTG6 PGA_DD PGA_SS net6 PGA_OUTP S1B PGA_S1 TG
.ends


* expanding   symbol:  ECG_Acquisition_IC/Design_Files/IC Design/Schematic/SEL/SEL.sym # of pins=9
** sym_path: Design_Files/IC Design/Schematic/SEL/SEL.sym
** sch_path: Design_Files/IC Design/Schematic/SEL/SEL.sch
.subckt SEL SEL_DD SEL_SS SEL_INTP SEL_INTN SEL_OUTN SEL_OUTP SEL_EXTP SEL_EXTN SEL_SEL
*.iopin SEL_DD
*.iopin SEL_SS
*.ipin SEL_INTP
*.ipin SEL_INTN
*.iopin SEL_OUTP
*.iopin SEL_OUTN
*.ipin SEL_EXTP
*.ipin SEL_EXTN
*.ipin SEL_SEL
xINV1 SEL_DD SEL_SS SEL_SEL SELB INV
xTG1 SEL_DD SEL_SS SEL_EXTP SEL_OUTP SEL_SEL SELB TG
xTG2 SEL_DD SEL_SS SEL_INTP SEL_OUTP SELB SEL_SEL TG
xTG3 SEL_DD SEL_SS SEL_EXTN SEL_OUTN SEL_SEL SELB TG
xTG4 SEL_DD SEL_SS SEL_INTN SEL_OUTN SELB SEL_SEL TG
.ends


* expanding   symbol:  ECG_Acquisition_IC/Design_Files/IC Design/Schematic/INA/INA.sym # of pins=13
** sym_path: Design_Files/IC Design/Schematic/INA/INA.sym
** sch_path: Design_Files/IC Design/Schematic/INA/INA.sch
.subckt INA INA_DD INA_SS INA_INP INA_INN INA_OUTN INA_BFDC INA_OUTP INA_BCMFB INA_REF INA_SEON
+ INA_SEOP INA_BSE1 INA_BSE2
*.iopin INA_DD
*.iopin INA_SS
*.ipin INA_INP
*.ipin INA_INN
*.opin INA_OUTP
*.iopin INA_BFDC
*.opin INA_OUTN
*.iopin INA_BCMFB
*.iopin INA_REF
*.iopin INA_BSE1
*.iopin INA_SEON
*.iopin INA_SEOP
*.iopin INA_BSE2
RFDFBP INA_FDINP INA_OUTN 40k m=1
xFDOTA1 INA_DD INA_SS INA_FDINP INA_FDINN INA_OUTN INA_BFDC INA_OUTP INA_BCMFB INA_REF INA_VOCM
+ FD_OTA
xSEOTA1 INA_DD INA_SS INA_INP INA_SEFP INA_SEOP INA_BSE1 SE_OTA
xSEOTA2 INA_DD INA_SS INA_INN INA_SEFN INA_SEON INA_BSE2 SE_OTA
RFDFBN INA_FDINN INA_OUTP 40k m=1
RFDINP INA_SEOP INA_FDINP 10k m=1
RFDINN INA_SEON INA_FDINN 10k m=1
RSEFP INA_SEOP INA_SEFP 118k m=1
RSEFN INA_SEON INA_SEFN 118k m=1
RSEG INA_SEFP INA_SEFN 4k m=1
.ends


* expanding   symbol:  ECG_Acquisition_IC/Design_Files/IC Design/Schematic/BUFFER/BUFFER.sym # of
*+ pins=9
** sym_path: Design_Files/IC Design/Schematic/BUFFER/BUFFER.sym
** sch_path: Design_Files/IC Design/Schematic/BUFFER/BUFFER.sch
.subckt BUFFER BUFFER_DD BUFFER_SS BUFFER_INP BUFFER_INN BUFFER_OUTN BUFFER_BFDC BUFFER_OUTP
+ BUFFER_BCMFB BUFFER_REF
*.iopin BUFFER_DD
*.iopin BUFFER_SS
*.ipin BUFFER_INP
*.ipin BUFFER_INN
*.opin BUFFER_OUTP
*.iopin BUFFER_BFDC
*.opin BUFFER_OUTN
*.iopin BUFFER_BCMFB
*.iopin BUFFER_REF
RFBP net1 BUFFER_OUTN 20k m=1
xFDOTA1 BUFFER_DD BUFFER_SS net1 net2 BUFFER_OUTN BUFFER_BFDC BUFFER_OUTP BUFFER_BCMFB BUFFER_REF
+ BUFFER_VOCM FD_OTA
RINN BUFFER_INN net2 20k m=1
RINP BUFFER_INP net1 20k m=1
RFBN net2 BUFFER_OUTP 20k m=1
.ends


* expanding   symbol:  ECG_Acquisition_IC/Design_Files/IC Design/Schematic/FD_OTA/FDOTA/FD_OTA.sym #
*+ of pins=10
** sym_path: Design_Files/IC Design/Schematic/FD_OTA/FDOTA/FD_OTA.sym
** sch_path: Design_Files/IC Design/Schematic/FD_OTA/FDOTA/FD_OTA.sch
.subckt FD_OTA FDOTA_DD FDOTA_SS FDOTA_INP FDOTA_INN FDOTA_OUTN FDOTA_BFDC FDOTA_OUTP FDOTA_BCMFB
+ FDOTA_REF FDOTA_VOCM
*.iopin FDOTA_DD
*.iopin FDOTA_SS
*.ipin FDOTA_INP
*.ipin FDOTA_INN
*.opin FDOTA_OUTP
*.iopin FDOTA_BFDC
*.opin FDOTA_OUTN
*.iopin FDOTA_BCMFB
*.iopin FDOTA_REF
*.iopin FDOTA_VOCM
R1 FDOTA_OUTP FDOTA_VOCM 100k m=1
R2 FDOTA_VOCM FDOTA_OUTN 100k m=1
C1 FDOTA_OUTP FDOTA_VOCM 50f m=1
C2 FDOTA_VOCM FDOTA_OUTN 50f m=1
xFDC1 FDOTA_DD FDOTA_SS FDOTA_INP FDOTA_INN FDOTA_OUTN FDOTA_BFDC FDOTA_OUTP FDOTA_VCMFB FDC
xCMFB1 FDOTA_DD FDOTA_SS FDOTA_VOCM FDOTA_REF FDOTA_VCMFB FDOTA_BCMFB CMFB
.ends


* expanding   symbol:  ECG_Acquisition_IC/Design_Files/IC Design/Schematic/TG/TG.sym # of pins=6
** sym_path: Design_Files/IC Design/Schematic/TG/TG.sym
** sch_path: Design_Files/IC Design/Schematic/TG/TG.sch
.subckt TG TG_DD TG_SS TG_A TG_B TG_SEL TG_SELB
*.iopin TG_DD
*.iopin TG_SS
*.iopin TG_A
*.iopin TG_B
*.ipin TG_SEL
*.ipin TG_SELB
XMTGP TG_B TG_SELB TG_A TG_DD pfet_03v3 L=0.5u W=10u nf=1 ad='int((nf+1)/2) * W/nf * 0.18u' as='int((nf+2)/2) * W/nf * 0.18u'
+ pd='2*int((nf+1)/2) * (W/nf + 0.18u)' ps='2*int((nf+2)/2) * (W/nf + 0.18u)' nrd='0.18u / W' nrs='0.18u / W'
+ sa=0 sb=0 sd=0 m=1
XMTGN TG_A TG_SEL TG_B TG_SS nfet_03v3 L=0.5u W=5u nf=1 ad='int((nf+1)/2) * W/nf * 0.18u' as='int((nf+2)/2) * W/nf * 0.18u'
+ pd='2*int((nf+1)/2) * (W/nf + 0.18u)' ps='2*int((nf+2)/2) * (W/nf + 0.18u)' nrd='0.18u / W' nrs='0.18u / W'
+ sa=0 sb=0 sd=0 m=1
.ends


* expanding   symbol:  ECG_Acquisition_IC/Design_Files/IC Design/Schematic/INV/INV.sym # of pins=4
** sym_path: Design_Files/IC Design/Schematic/INV/INV.sym
** sch_path: Design_Files/IC Design/Schematic/INV/INV.sch
.subckt INV INV_DD INV_SS INV_IN INV_OUT
*.iopin INV_DD
*.iopin INV_SS
*.ipin INV_IN
*.opin INV_OUT
XMINVP INV_OUT INV_IN INV_DD INV_DD pfet_03v3 L=0.5u W=2u nf=1 ad='int((nf+1)/2) * W/nf * 0.18u' as='int((nf+2)/2) * W/nf * 0.18u'
+ pd='2*int((nf+1)/2) * (W/nf + 0.18u)' ps='2*int((nf+2)/2) * (W/nf + 0.18u)' nrd='0.18u / W' nrs='0.18u / W'
+ sa=0 sb=0 sd=0 m=1
XMINVN INV_OUT INV_IN INV_SS INV_SS nfet_03v3 L=0.5u W=1u nf=1 ad='int((nf+1)/2) * W/nf * 0.18u' as='int((nf+2)/2) * W/nf * 0.18u'
+ pd='2*int((nf+1)/2) * (W/nf + 0.18u)' ps='2*int((nf+2)/2) * (W/nf + 0.18u)' nrd='0.18u / W' nrs='0.18u / W'
+ sa=0 sb=0 sd=0 m=1
.ends


* expanding   symbol:  ECG_Acquisition_IC/Design_Files/IC Design/Schematic/SE_OTA/SE_OTA.sym # of
*+ pins=6
** sym_path: Design_Files/IC Design/Schematic/SE_OTA/SE_OTA.sym
** sch_path: Design_Files/IC Design/Schematic/SE_OTA/SE_OTA.sch
.subckt SE_OTA SEOTA_DD SEOTA_SS SEOTA_INP SEOTA_INN SEOTA_OUT SEOTA_B
*.iopin SEOTA_DD
*.iopin SEOTA_SS
*.ipin SEOTA_INP
*.ipin SEOTA_INN
*.opin SEOTA_OUT
*.iopin SEOTA_B
XM3 net4 net4 SEOTA_DD SEOTA_DD pfet_03v3 L=4u W=1u nf=1 ad='int((nf+1)/2) * W/nf * 0.18u' as='int((nf+2)/2) * W/nf * 0.18u'
+ pd='2*int((nf+1)/2) * (W/nf + 0.18u)' ps='2*int((nf+2)/2) * (W/nf + 0.18u)' nrd='0.18u / W' nrs='0.18u / W'
+ sa=0 sb=0 sd=0 m=60
XM7 SEOTA_OUT SEOTA_B SEOTA_SS SEOTA_SS nfet_03v3 L=0.5u W=1u nf=1 ad='int((nf+1)/2) * W/nf * 0.18u'
+ as='int((nf+2)/2) * W/nf * 0.18u' pd='2*int((nf+1)/2) * (W/nf + 0.18u)' ps='2*int((nf+2)/2) * (W/nf + 0.18u)'
+ nrd='0.18u / W' nrs='0.18u / W' sa=0 sb=0 sd=0 m=100
Rz net1 net2 3.8k m=1
XM5 net3 SEOTA_B SEOTA_SS SEOTA_SS nfet_03v3 L=2u W=1u nf=1 ad='int((nf+1)/2) * W/nf * 0.18u' as='int((nf+2)/2) * W/nf * 0.18u'
+ pd='2*int((nf+1)/2) * (W/nf + 0.18u)' ps='2*int((nf+2)/2) * (W/nf + 0.18u)' nrd='0.18u / W' nrs='0.18u / W'
+ sa=0 sb=0 sd=0 m=10
XM6 SEOTA_OUT net1 SEOTA_DD SEOTA_DD pfet_03v3 L=0.5u W=1u nf=1 ad='int((nf+1)/2) * W/nf * 0.18u' as='int((nf+2)/2) * W/nf * 0.18u'
+ pd='2*int((nf+1)/2) * (W/nf + 0.18u)' ps='2*int((nf+2)/2) * (W/nf + 0.18u)' nrd='0.18u / W' nrs='0.18u / W'
+ sa=0 sb=0 sd=0 m=400
XM8 SEOTA_B SEOTA_B SEOTA_SS SEOTA_SS nfet_03v3 L=2u W=1u nf=1 ad='int((nf+1)/2) * W/nf * 0.18u' as='int((nf+2)/2) * W/nf * 0.18u'
+ pd='2*int((nf+1)/2) * (W/nf + 0.18u)' ps='2*int((nf+2)/2) * (W/nf + 0.18u)' nrd='0.18u / W' nrs='0.18u / W'
+ sa=0 sb=0 sd=0 m=20
Cc net2 SEOTA_OUT 2p m=1
XM4 net1 net4 SEOTA_DD SEOTA_DD pfet_03v3 L=4u W=1u nf=1 ad='int((nf+1)/2) * W/nf * 0.18u' as='int((nf+2)/2) * W/nf * 0.18u'
+ pd='2*int((nf+1)/2) * (W/nf + 0.18u)' ps='2*int((nf+2)/2) * (W/nf + 0.18u)' nrd='0.18u / W' nrs='0.18u / W'
+ sa=0 sb=0 sd=0 m=60
XM1 net4 SEOTA_INN net3 SEOTA_SS nfet_03v3 L=4u W=1u nf=1 ad='int((nf+1)/2) * W/nf * 0.18u' as='int((nf+2)/2) * W/nf * 0.18u'
+ pd='2*int((nf+1)/2) * (W/nf + 0.18u)' ps='2*int((nf+2)/2) * (W/nf + 0.18u)' nrd='0.18u / W' nrs='0.18u / W'
+ sa=0 sb=0 sd=0 m=400
XM2 net1 SEOTA_INP net3 SEOTA_SS nfet_03v3 L=4u W=1u nf=1 ad='int((nf+1)/2) * W/nf * 0.18u' as='int((nf+2)/2) * W/nf * 0.18u'
+ pd='2*int((nf+1)/2) * (W/nf + 0.18u)' ps='2*int((nf+2)/2) * (W/nf + 0.18u)' nrd='0.18u / W' nrs='0.18u / W'
+ sa=0 sb=0 sd=0 m=400
.ends


* expanding   symbol:  ECG_Acquisition_IC/Design_Files/IC Design/Schematic/FD_OTA/FDC/FDC.sym # of
*+ pins=8
** sym_path: Design_Files/IC Design/Schematic/FD_OTA/FDC/FDC.sym
** sch_path: Design_Files/IC Design/Schematic/FD_OTA/FDC/FDC.sch
.subckt FDC FDC_DD FDC_SS FDC_INP FDC_INN FDC_OUTN FDC_B FDC_OUTP FDC_CMFB
*.iopin FDC_DD
*.iopin FDC_SS
*.ipin FDC_INP
*.ipin FDC_INN
*.opin FDC_OUTP
*.iopin FDC_B
*.opin FDC_OUTN
*.iopin FDC_CMFB
XM3 net4 FDC_CMFB FDC_DD FDC_DD pfet_03v3 L=2u W=1u nf=1 ad='int((nf+1)/2) * W/nf * 0.18u' as='int((nf+2)/2) * W/nf * 0.18u'
+ pd='2*int((nf+1)/2) * (W/nf + 0.18u)' ps='2*int((nf+2)/2) * (W/nf + 0.18u)' nrd='0.18u / W' nrs='0.18u / W'
+ sa=0 sb=0 sd=0 m=200
XM8 FDC_OUTP FDC_B FDC_SS FDC_SS nfet_03v3 L=0.5u W=1u nf=1 ad='int((nf+1)/2) * W/nf * 0.18u' as='int((nf+2)/2) * W/nf * 0.18u'
+ pd='2*int((nf+1)/2) * (W/nf + 0.18u)' ps='2*int((nf+2)/2) * (W/nf + 0.18u)' nrd='0.18u / W' nrs='0.18u / W'
+ sa=0 sb=0 sd=0 m=100
Rz net1 net2 3.5k m=1
XM5 net3 FDC_B FDC_SS FDC_SS nfet_03v3 L=2u W=1u nf=1 ad='int((nf+1)/2) * W/nf * 0.18u' as='int((nf+2)/2) * W/nf * 0.18u'
+ pd='2*int((nf+1)/2) * (W/nf + 0.18u)' ps='2*int((nf+2)/2) * (W/nf + 0.18u)' nrd='0.18u / W' nrs='0.18u / W'
+ sa=0 sb=0 sd=0 m=10
XM6 FDC_OUTP net1 FDC_DD FDC_DD pfet_03v3 L=0.5u W=1u nf=1 ad='int((nf+1)/2) * W/nf * 0.18u' as='int((nf+2)/2) * W/nf * 0.18u'
+ pd='2*int((nf+1)/2) * (W/nf + 0.18u)' ps='2*int((nf+2)/2) * (W/nf + 0.18u)' nrd='0.18u / W' nrs='0.18u / W'
+ sa=0 sb=0 sd=0 m=200
XM10 FDC_B FDC_B FDC_SS FDC_SS nfet_03v3 L=2u W=1u nf=1 ad='int((nf+1)/2) * W/nf * 0.18u' as='int((nf+2)/2) * W/nf * 0.18u'
+ pd='2*int((nf+1)/2) * (W/nf + 0.18u)' ps='2*int((nf+2)/2) * (W/nf + 0.18u)' nrd='0.18u / W' nrs='0.18u / W'
+ sa=0 sb=0 sd=0 m=20
Cc net2 FDC_OUTP 2.5p m=1
XM9 FDC_OUTN FDC_B FDC_SS FDC_SS nfet_03v3 L=0.5u W=1u nf=1 ad='int((nf+1)/2) * W/nf * 0.18u' as='int((nf+2)/2) * W/nf * 0.18u'
+ pd='2*int((nf+1)/2) * (W/nf + 0.18u)' ps='2*int((nf+2)/2) * (W/nf + 0.18u)' nrd='0.18u / W' nrs='0.18u / W'
+ sa=0 sb=0 sd=0 m=100
Rz1 net4 net5 3.5k m=1
XM7 FDC_OUTN net4 FDC_DD FDC_DD pfet_03v3 L=0.5u W=1u nf=1 ad='int((nf+1)/2) * W/nf * 0.18u' as='int((nf+2)/2) * W/nf * 0.18u'
+ pd='2*int((nf+1)/2) * (W/nf + 0.18u)' ps='2*int((nf+2)/2) * (W/nf + 0.18u)' nrd='0.18u / W' nrs='0.18u / W'
+ sa=0 sb=0 sd=0 m=200
Cc1 net5 FDC_OUTN 2.5p m=1
XM4 net1 FDC_CMFB FDC_DD FDC_DD pfet_03v3 L=2u W=1u nf=1 ad='int((nf+1)/2) * W/nf * 0.18u' as='int((nf+2)/2) * W/nf * 0.18u'
+ pd='2*int((nf+1)/2) * (W/nf + 0.18u)' ps='2*int((nf+2)/2) * (W/nf + 0.18u)' nrd='0.18u / W' nrs='0.18u / W'
+ sa=0 sb=0 sd=0 m=200
XM1 net4 FDC_INN net3 FDC_SS nfet_03v3 L=2u W=1u nf=1 ad='int((nf+1)/2) * W/nf * 0.18u' as='int((nf+2)/2) * W/nf * 0.18u'
+ pd='2*int((nf+1)/2) * (W/nf + 0.18u)' ps='2*int((nf+2)/2) * (W/nf + 0.18u)' nrd='0.18u / W' nrs='0.18u / W'
+ sa=0 sb=0 sd=0 m=200
XM2 net1 FDC_INP net3 FDC_SS nfet_03v3 L=2u W=1u nf=1 ad='int((nf+1)/2) * W/nf * 0.18u' as='int((nf+2)/2) * W/nf * 0.18u'
+ pd='2*int((nf+1)/2) * (W/nf + 0.18u)' ps='2*int((nf+2)/2) * (W/nf + 0.18u)' nrd='0.18u / W' nrs='0.18u / W'
+ sa=0 sb=0 sd=0 m=200
.ends


* expanding   symbol:  ECG_Acquisition_IC/Design_Files/IC Design/Schematic/FD_OTA/CMFB/CMFB.sym # of
*+ pins=6
** sym_path: Design_Files/IC Design/Schematic/FD_OTA/CMFB/CMFB.sym
** sch_path: Design_Files/IC Design/Schematic/FD_OTA/CMFB/CMFB.sch
.subckt CMFB CMFB_DD CMFB_SS CMFB_IN CMFB_REF CMFB_OUT CMFB_B
*.iopin CMFB_DD
*.iopin CMFB_SS
*.ipin CMFB_IN
*.ipin CMFB_REF
*.opin CMFB_OUT
*.iopin CMFB_B
XM4 CMFB_OUT CMFB_OUT CMFB_DD CMFB_DD pfet_03v3 L=0.5u W=1u nf=1 ad='int((nf+1)/2) * W/nf * 0.18u' as='int((nf+2)/2) * W/nf * 0.18u'
+ pd='2*int((nf+1)/2) * (W/nf + 0.18u)' ps='2*int((nf+2)/2) * (W/nf + 0.18u)' nrd='0.18u / W' nrs='0.18u / W'
+ sa=0 sb=0 sd=0 m=77
XM3 net2 net2 CMFB_DD CMFB_DD pfet_03v3 L=0.5u W=1u nf=1 ad='int((nf+1)/2) * W/nf * 0.18u' as='int((nf+2)/2) * W/nf * 0.18u'
+ pd='2*int((nf+1)/2) * (W/nf + 0.18u)' ps='2*int((nf+2)/2) * (W/nf + 0.18u)' nrd='0.18u / W' nrs='0.18u / W'
+ sa=0 sb=0 sd=0 m=77
XM1 net2 CMFB_REF net1 CMFB_SS nfet_03v3 L=0.5u W=1u nf=1 ad='int((nf+1)/2) * W/nf * 0.18u' as='int((nf+2)/2) * W/nf * 0.18u'
+ pd='2*int((nf+1)/2) * (W/nf + 0.18u)' ps='2*int((nf+2)/2) * (W/nf + 0.18u)' nrd='0.18u / W' nrs='0.18u / W'
+ sa=0 sb=0 sd=0 m=5
XM2 CMFB_OUT CMFB_IN net1 CMFB_SS nfet_03v3 L=0.5u W=1u nf=1 ad='int((nf+1)/2) * W/nf * 0.18u' as='int((nf+2)/2) * W/nf * 0.18u'
+ pd='2*int((nf+1)/2) * (W/nf + 0.18u)' ps='2*int((nf+2)/2) * (W/nf + 0.18u)' nrd='0.18u / W' nrs='0.18u / W'
+ sa=0 sb=0 sd=0 m=5
XM5 net1 CMFB_B CMFB_SS CMFB_SS nfet_03v3 L=2u W=1u nf=1 ad='int((nf+1)/2) * W/nf * 0.18u' as='int((nf+2)/2) * W/nf * 0.18u'
+ pd='2*int((nf+1)/2) * (W/nf + 0.18u)' ps='2*int((nf+2)/2) * (W/nf + 0.18u)' nrd='0.18u / W' nrs='0.18u / W'
+ sa=0 sb=0 sd=0 m=20
XM10 CMFB_B CMFB_B CMFB_SS CMFB_SS nfet_03v3 L=2u W=1u nf=1 ad='int((nf+1)/2) * W/nf * 0.18u' as='int((nf+2)/2) * W/nf * 0.18u'
+ pd='2*int((nf+1)/2) * (W/nf + 0.18u)' ps='2*int((nf+2)/2) * (W/nf + 0.18u)' nrd='0.18u / W' nrs='0.18u / W'
+ sa=0 sb=0 sd=0 m=20
.ends

.end
